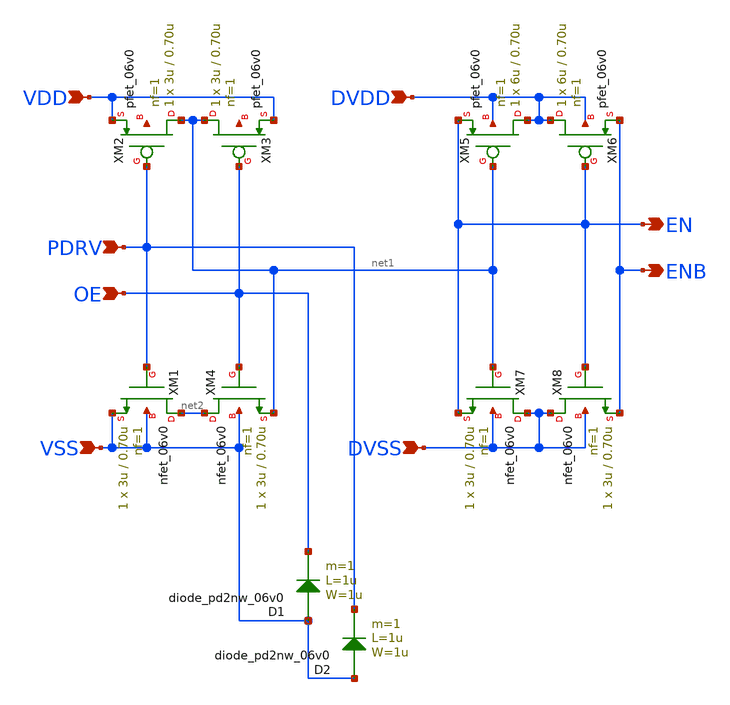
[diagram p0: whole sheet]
** sch_path: gf180mcu_fd_io__bi_24t/comp018green_out_sigbuf_oe.sch
**.subckt comp018green_out_sigbuf_oe PDRV OE VDD VSS DVDD DVSS EN ENB
*.ipin PDRV
*.ipin OE
*.ipin VDD
*.ipin VSS
*.ipin DVDD
*.ipin DVSS
*.opin EN
*.opin ENB
XM1 net2 PDRV VSS VSS nfet_06v0 L=0.70u W=3u nf=1 ad='int((nf+1)/2) * W/nf * 0.18u' as='int((nf+2)/2) * W/nf * 0.18u'
+ pd='2*int((nf+1)/2) * (W/nf + 0.18u)' ps='2*int((nf+2)/2) * (W/nf + 0.18u)' nrd='0.18u / W' nrs='0.18u / W'
+ sa=0 sb=0 sd=0 m=1
XM2 net1 PDRV VDD net3 pfet_06v0 L=0.70u W=3u nf=1 ad='int((nf+1)/2) * W/nf * 0.18u' as='int((nf+2)/2) * W/nf * 0.18u'
+ pd='2*int((nf+1)/2) * (W/nf + 0.18u)' ps='2*int((nf+2)/2) * (W/nf + 0.18u)' nrd='0.18u / W' nrs='0.18u / W'
+ sa=0 sb=0 sd=0 m=1
XM3 net1 OE VDD net4 pfet_06v0 L=0.70u W=3u nf=1 ad='int((nf+1)/2) * W/nf * 0.18u' as='int((nf+2)/2) * W/nf * 0.18u'
+ pd='2*int((nf+1)/2) * (W/nf + 0.18u)' ps='2*int((nf+2)/2) * (W/nf + 0.18u)' nrd='0.18u / W' nrs='0.18u / W'
+ sa=0 sb=0 sd=0 m=1
XM4 net2 OE net1 VSS nfet_06v0 L=0.70u W=3u nf=1 ad='int((nf+1)/2) * W/nf * 0.18u' as='int((nf+2)/2) * W/nf * 0.18u'
+ pd='2*int((nf+1)/2) * (W/nf + 0.18u)' ps='2*int((nf+2)/2) * (W/nf + 0.18u)' nrd='0.18u / W' nrs='0.18u / W'
+ sa=0 sb=0 sd=0 m=1
XM5 DVDD net1 EN DVDD pfet_06v0 L=0.70u W=6u nf=1 ad='int((nf+1)/2) * W/nf * 0.18u' as='int((nf+2)/2) * W/nf * 0.18u'
+ pd='2*int((nf+1)/2) * (W/nf + 0.18u)' ps='2*int((nf+2)/2) * (W/nf + 0.18u)' nrd='0.18u / W' nrs='0.18u / W'
+ sa=0 sb=0 sd=0 m=1
XM6 DVDD EN ENB DVDD pfet_06v0 L=0.70u W=6u nf=1 ad='int((nf+1)/2) * W/nf * 0.18u' as='int((nf+2)/2) * W/nf * 0.18u'
+ pd='2*int((nf+1)/2) * (W/nf + 0.18u)' ps='2*int((nf+2)/2) * (W/nf + 0.18u)' nrd='0.18u / W' nrs='0.18u / W'
+ sa=0 sb=0 sd=0 m=1
XM7 DVSS net1 EN DVSS nfet_06v0 L=0.70u W=3u nf=1 ad='int((nf+1)/2) * W/nf * 0.18u' as='int((nf+2)/2) * W/nf * 0.18u'
+ pd='2*int((nf+1)/2) * (W/nf + 0.18u)' ps='2*int((nf+2)/2) * (W/nf + 0.18u)' nrd='0.18u / W' nrs='0.18u / W'
+ sa=0 sb=0 sd=0 m=1
XM8 DVSS EN ENB DVSS nfet_06v0 L=0.70u W=3u nf=1 ad='int((nf+1)/2) * W/nf * 0.18u' as='int((nf+2)/2) * W/nf * 0.18u'
+ pd='2*int((nf+1)/2) * (W/nf + 0.18u)' ps='2*int((nf+2)/2) * (W/nf + 0.18u)' nrd='0.18u / W' nrs='0.18u / W'
+ sa=0 sb=0 sd=0 m=1
D1 VSS OE diode_pd2nw_06v0 area='1u * 1u ' pj='2*1u + 2*1u ' m=1
D2 VSS PDRV diode_pd2nw_06v0 area='1u * 1u ' pj='2*1u + 2*1u ' m=1
**.ends
.end
